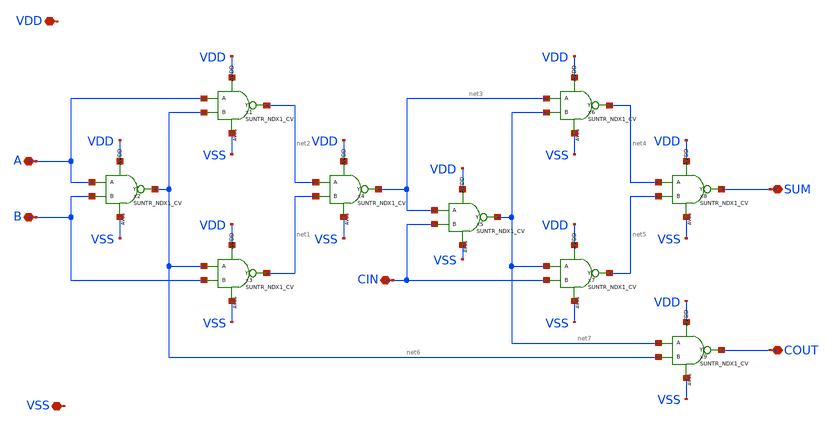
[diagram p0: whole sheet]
** sch_path: design/CNR_GR03_SKY130NM/1_BIT_ADDER.sch
**.subckt 1_BIT_ADDER A B SUM COUT CIN VDD VSS
*.iopin A
*.iopin B
*.iopin SUM
*.iopin COUT
*.iopin CIN
*.iopin VDD
*.iopin VSS
x2 A B net6 VDD VSS SUNTR_NDX1_CV
x1 A net6 net2 VDD VSS SUNTR_NDX1_CV
x3 net6 B net1 VDD VSS SUNTR_NDX1_CV
x4 net2 net1 net3 VDD VSS SUNTR_NDX1_CV
x5 net3 CIN net7 VDD VSS SUNTR_NDX1_CV
x6 net3 net7 net4 VDD VSS SUNTR_NDX1_CV
x7 net7 CIN net5 VDD VSS SUNTR_NDX1_CV
x8 net4 net5 SUM VDD VSS SUNTR_NDX1_CV
x9 net7 net6 COUT VDD VSS SUNTR_NDX1_CV
**.ends
.end
